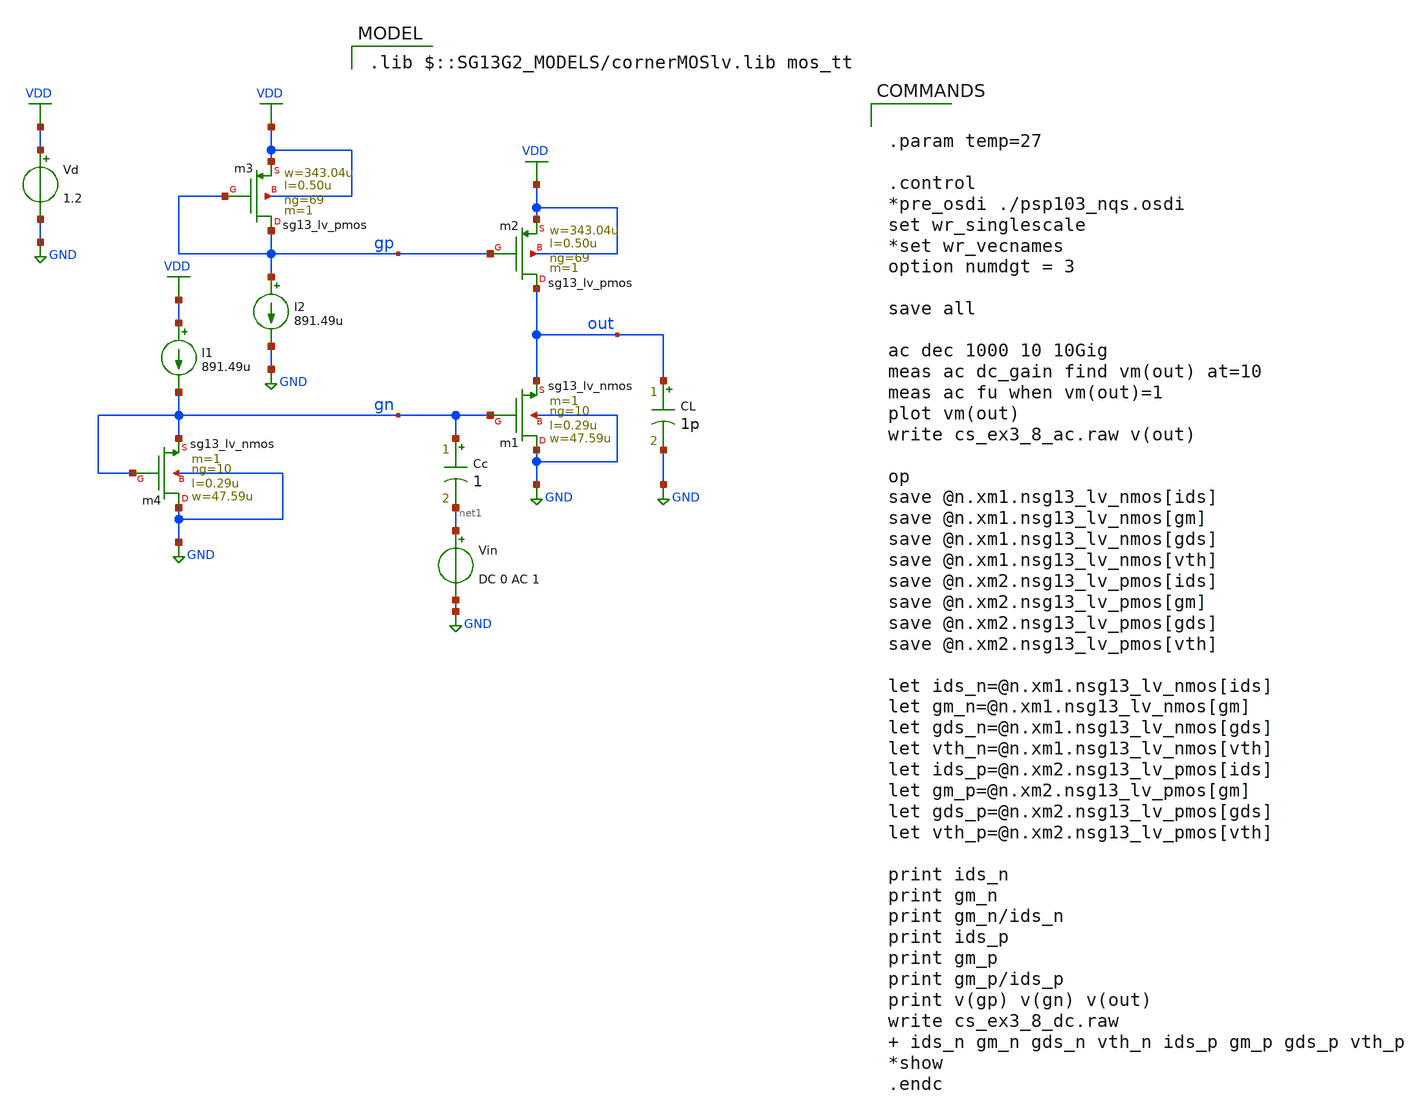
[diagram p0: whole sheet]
** sch_path: 03_design_examples/examples/src/CS_ex3_8.sch
**.subckt CS_ex3_8
Xm1 GND gn out GND sg13_lv_nmos w=47.59u l=0.29u ng=10 m=1 mm_ok=1
Vin net1 GND DC 0 AC 1
Vd VDD GND 1.2
CL out GND 1p m=1
Xm2 out gp VDD VDD sg13_lv_pmos w=343.04u l=0.50u ng=69 m=1 mm_ok=1
Xm3 gp gp VDD VDD sg13_lv_pmos w=343.04u l=0.50u ng=69 m=1 mm_ok=1
Xm4 GND gn gn GND sg13_lv_nmos w=47.59u l=0.29u ng=10 m=1 mm_ok=1
I1 VDD gn 891.49u
I2 gp GND 891.49u
Cc gn net1 1 m=1
**** begin user architecture code
 .lib $::SG13G2_MODELS/cornerMOSlv.lib mos_tt



.param temp=27

.control
*pre_osdi ./psp103_nqs.osdi
set wr_singlescale
*set wr_vecnames
option numdgt = 3

save all

ac dec 1000 10 10Gig
meas ac dc_gain find vm(out) at=10
meas ac fu when vm(out)=1
plot vm(out)
write cs_ex3_8_ac.raw v(out)

op
save @n.xm1.nsg13_lv_nmos[ids]
save @n.xm1.nsg13_lv_nmos[gm]
save @n.xm1.nsg13_lv_nmos[gds]
save @n.xm1.nsg13_lv_nmos[vth]
save @n.xm2.nsg13_lv_pmos[ids]
save @n.xm2.nsg13_lv_pmos[gm]
save @n.xm2.nsg13_lv_pmos[gds]
save @n.xm2.nsg13_lv_pmos[vth]

let ids_n=@n.xm1.nsg13_lv_nmos[ids]
let gm_n=@n.xm1.nsg13_lv_nmos[gm]
let gds_n=@n.xm1.nsg13_lv_nmos[gds]
let vth_n=@n.xm1.nsg13_lv_nmos[vth]
let ids_p=@n.xm2.nsg13_lv_pmos[ids]
let gm_p=@n.xm2.nsg13_lv_pmos[gm]
let gds_p=@n.xm2.nsg13_lv_pmos[gds]
let vth_p=@n.xm2.nsg13_lv_pmos[vth]

print ids_n
print gm_n
print gm_n/ids_n
print ids_p
print gm_p
print gm_p/ids_p
print v(gp) v(gn) v(out)
write cs_ex3_8_dc.raw   ids_n gm_n gds_n vth_n ids_p gm_p gds_p vth_p
*show
.endc


**** end user architecture code
**.ends
.GLOBAL GND
.GLOBAL VDD
.end
